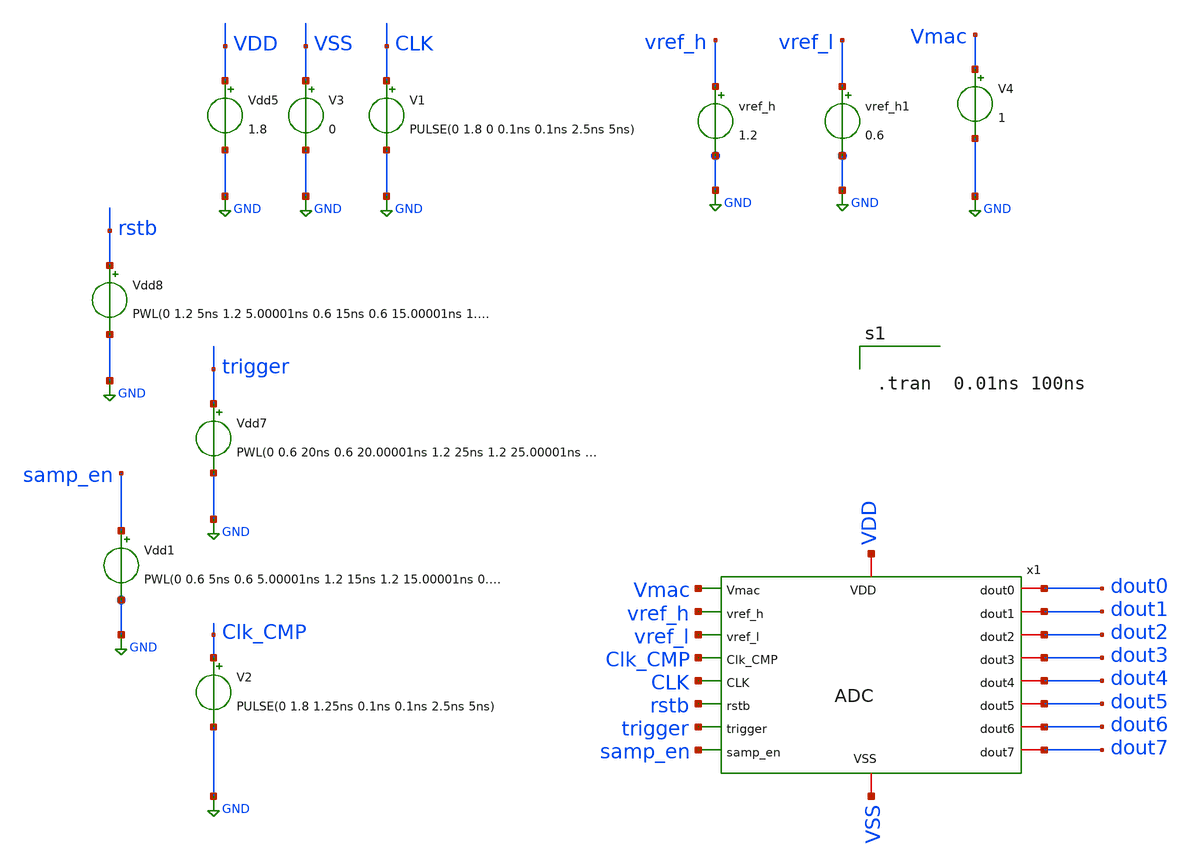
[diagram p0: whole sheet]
** sch_path: ADC_sym_TB.sch
**.subckt ADC_sym_TB
vref_h vref_h GND 1.2
Vdd5 VDD GND 1.8
V1 CLK GND PULSE(0 1.8 0 0.1ns 0.1ns 2.5ns 5ns)
V3 VSS GND 0
Vdd7 trigger GND PWL(0 0.6 20ns 0.6 20.00001ns 1.2 25ns 1.2 25.00001ns 0.6 )
Vdd8 rstb GND PWL(0 1.2 5ns 1.2 5.00001ns 0.6 15ns 0.6 15.00001ns 1.2 )
V4 Vmac GND 1
V2 Clk_CMP GND PULSE(0 1.8 1.25ns 0.1ns 0.1ns 2.5ns 5ns)
Vdd1 samp_en GND PWL(0 0.6 5ns 0.6 5.00001ns 1.2 15ns 1.2 15.00001ns 0.6 )
vref_h1 vref_l GND 0.6
x1 dout0 dout1 VSS vref_h dout2 VDD vref_l trigger dout3 CLK dout4 rstb Clk_CMP samp_en dout5 Vmac
+ dout6 dout7 ADC
**** begin user architecture code

** opencircuitdesign pdks install
.lib $::SKYWATER_MODELS/sky130.lib.spice tt
.include $::SKYWATER_STDCELLS/sky130_fd_sc_hd.spice



.tran  0.01ns 100ns



**** end user architecture code
**.ends
.GLOBAL GND
.end
